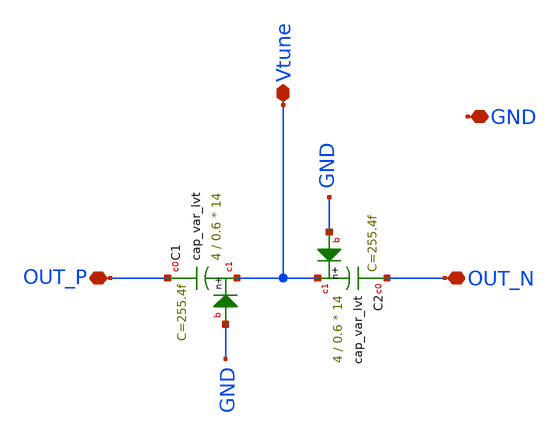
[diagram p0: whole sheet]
** sch_path: xschem/cap_var.sch
**.subckt cap_var OUT_P OUT_N Vtune GND
*.iopin OUT_P
*.iopin OUT_N
*.iopin Vtune
*.iopin GND
XC1 OUT_P Vtune GND sky130_fd_pr__cap_var_lvt W=4 L=0.6 VM=14 m=14
XC2 OUT_N Vtune GND sky130_fd_pr__cap_var_lvt W=4 L=0.6 VM=14 m=14
**.ends
.end
